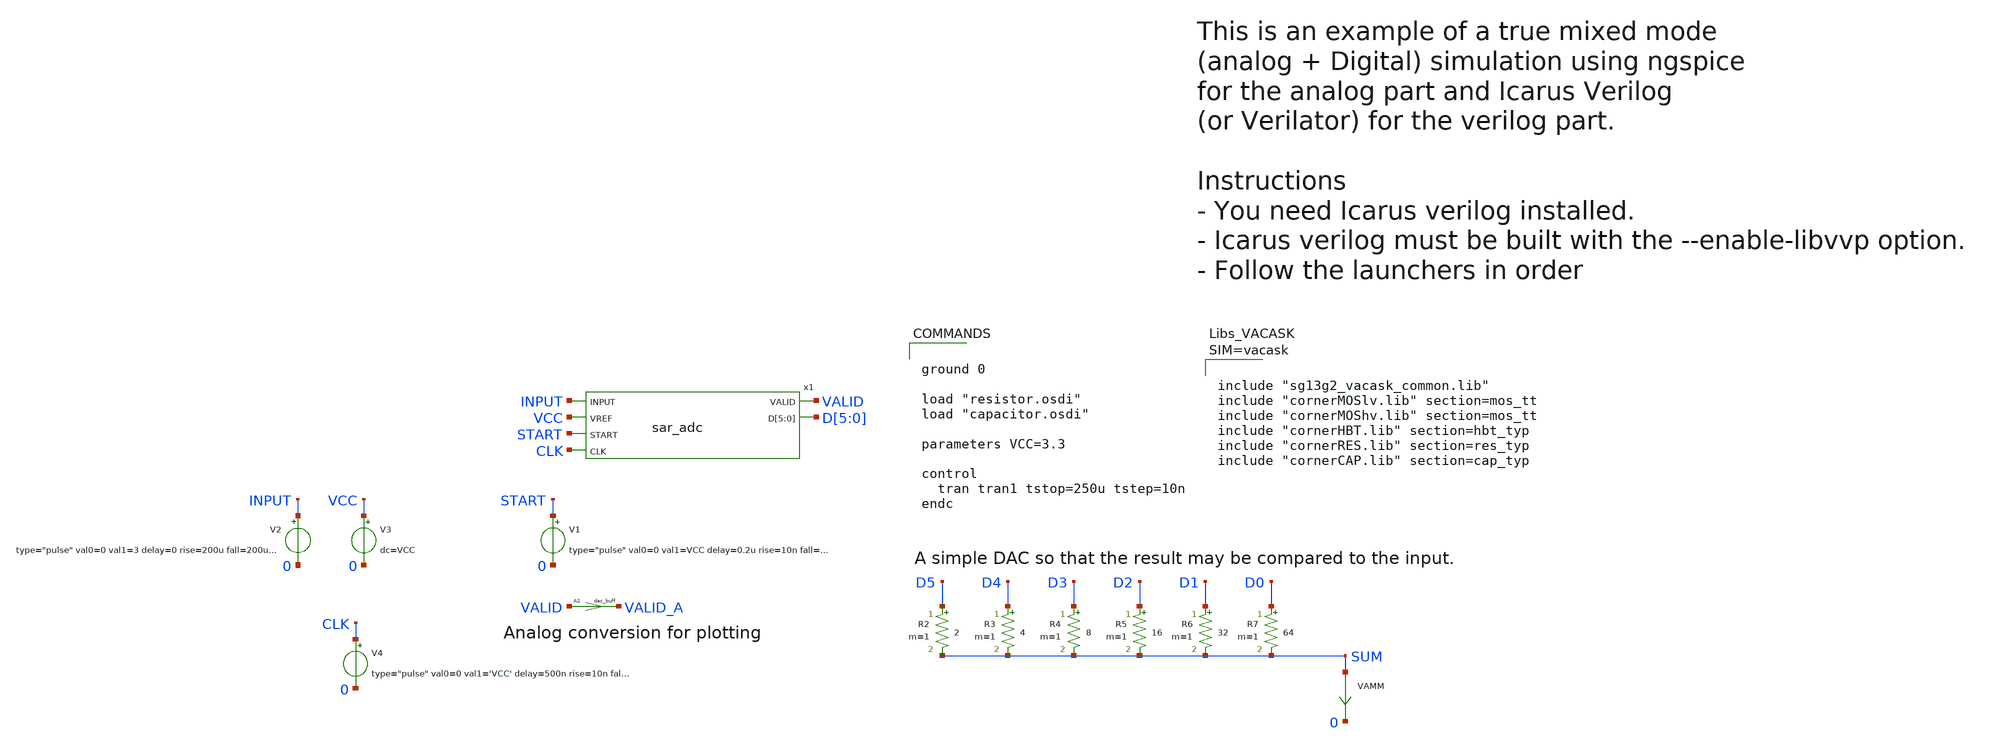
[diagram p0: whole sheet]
** sch_path: demo/cosim/test_new/vacask_cosim_hier/final_folder/tb_sar_adc.sch
**.subckt tb_sar_adc
VAMM SUM 0 0
R2 D5 SUM 2 m=1
R3 D4 SUM 4 m=1
R4 D3 SUM 8 m=1
R5 D2 SUM 16 m=1
R6 D1 SUM 32 m=1
R7 D0 SUM 64 m=1
A2 [ VALID ] [ VALID_A ] dac_buff
V3 VCC 0 dc=VCC
V2 INPUT 0 type="pulse" val0=0 val1=3 delay=0 rise=200u fall=200u width=1u period=402u
V1 START 0 type="pulse" val0=0 val1=VCC delay=0.2u rise=10n fall=10n width=1.3u period=10u
V4 CLK 0 type="pulse" val0=0 val1='VCC' delay=500n rise=10n fall=10n width=490n period=1u
x1 INPUT VCC START VALID D[5] D[4] D[3] D[2] D[1] D[0] CLK sar_adc
**** begin user architecture code


ground 0

load "resistor.osdi"
load "capacitor.osdi"

parameters VCC=3.3

control
  tran tran1 tstop=250u tstep=10n
endc





**** end user architecture code
**.ends
**** begin user architecture code
.model dac_buff dac_bridge input_load=1e-15 t_rise=10n t_fall=10n  out_low=0 out_high=3.3
**** end user architecture code
.end
